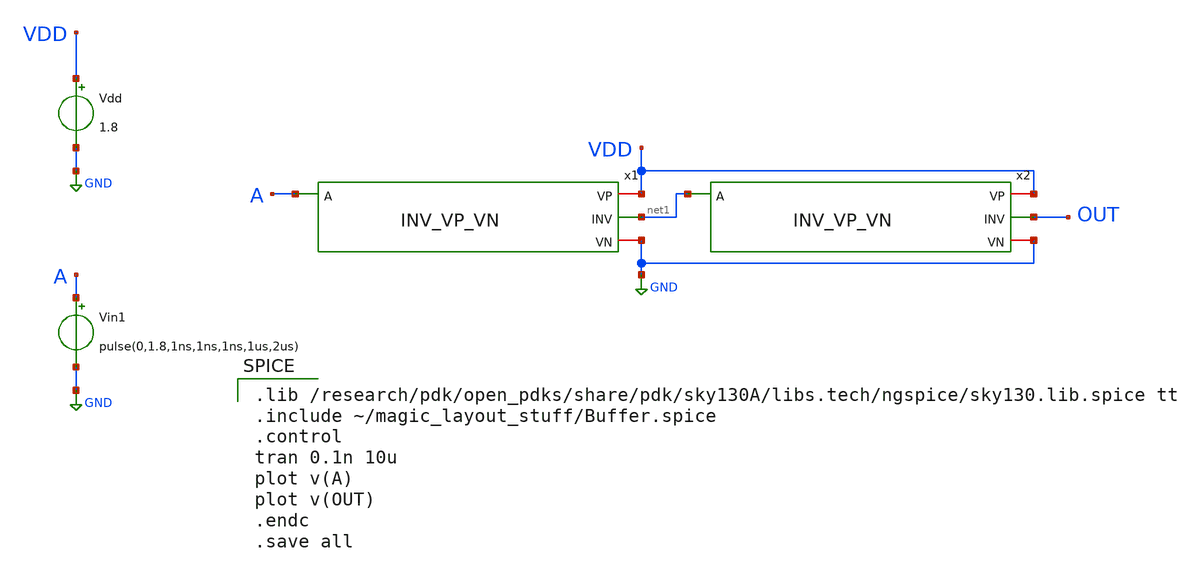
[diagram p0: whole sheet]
** sch_path: skywater_stuff/Buffer_sim.sch
**.subckt Buffer_sim
Vdd VDD GND 1.8
Vin1 A GND pulse(0,1.8,1ns,1ns,1ns,1us,2us)
x1 VDD A net1 GND INV_VP_VN
x2 VDD net1 OUT GND INV_VP_VN
**** begin user architecture code

.lib /research/pdk/open_pdks/share/pdk/sky130A/libs.tech/ngspice/sky130.lib.spice tt
.include ~/magic_layout_stuff/Buffer.spice
.control
tran 0.1n 10u
plot v(A)
plot v(OUT)
.endc
.save all

**** end user architecture code
**.ends
.GLOBAL GND
.end
